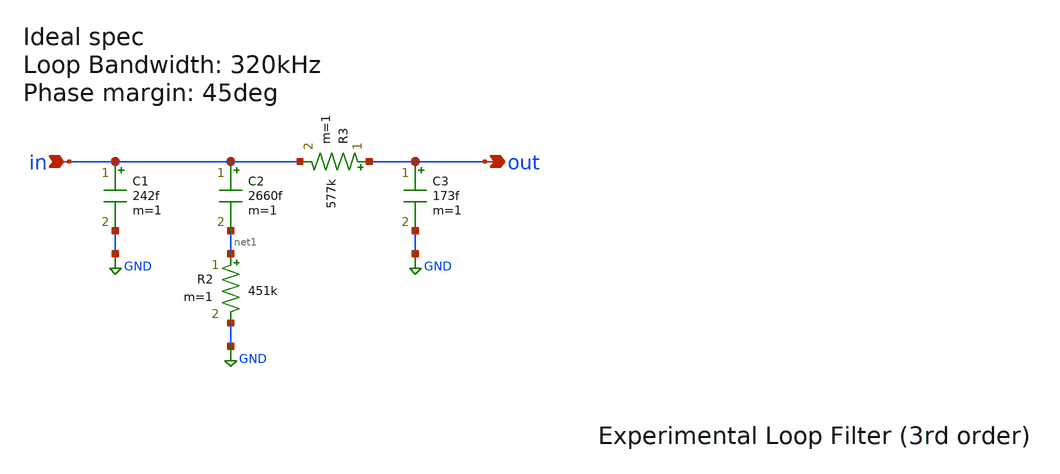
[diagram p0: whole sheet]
** sch_path: PLL/xschem/lf.sch
**.subckt lf in out
*.ipin in
*.opin out
R2 net1 GND 451k m=1
C1 in GND 242f m=1
C2 in net1 2660f m=1
R3 out in 577k m=1
C3 out GND 173f m=1
**.ends
.GLOBAL GND
.end
